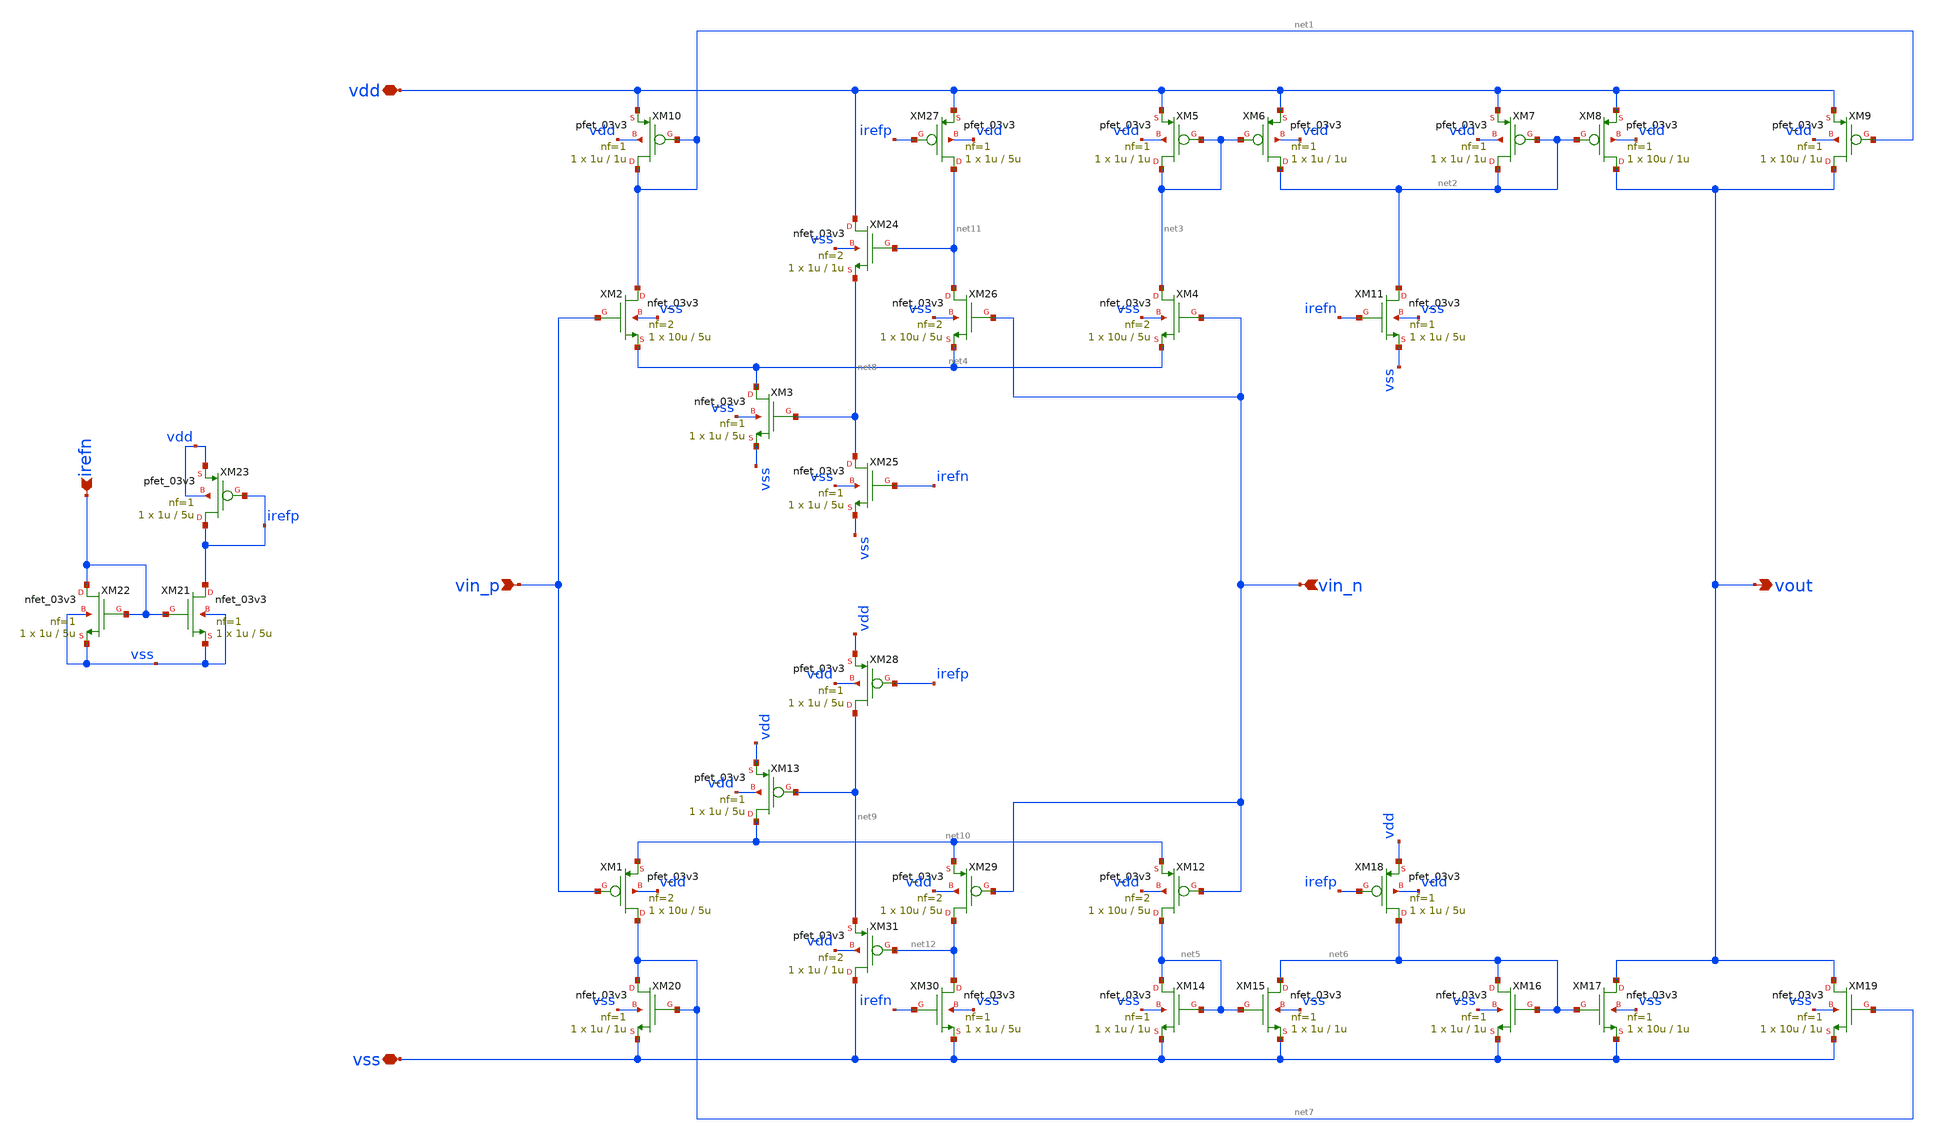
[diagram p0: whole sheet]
** sch_path: Tobias/2026 07 14 Intermediate Results/analogbuffer/analogbuffer-openloop.sch
**.subckt analogbuffer-openloop vdd vss vin_p vout irefn vin_n
*.iopin vdd
*.iopin vss
*.ipin vin_p
*.opin vout
*.ipin irefn
*.ipin vin_n
XM1 net7 vin_p net10 vdd pfet_03v3 L=5u W=10u nf=2 ad='int((nf+1)/2) * W/nf * 0.18u' as='int((nf+2)/2) * W/nf * 0.18u'
+ pd='2*int((nf+1)/2) * (W/nf + 0.18u)' ps='2*int((nf+2)/2) * (W/nf + 0.18u)' nrd='0.18u / W' nrs='0.18u / W'
+ sa=0 sb=0 sd=0 m=1
XM2 net1 vin_p net4 vss nfet_03v3 L=5u W=10u nf=2 ad='int((nf+1)/2) * W/nf * 0.18u' as='int((nf+2)/2) * W/nf * 0.18u'
+ pd='2*int((nf+1)/2) * (W/nf + 0.18u)' ps='2*int((nf+2)/2) * (W/nf + 0.18u)' nrd='0.18u / W' nrs='0.18u / W'
+ sa=0 sb=0 sd=0 m=1
XM3 net4 net8 vss vss nfet_03v3 L=5u W=1u nf=1 ad='int((nf+1)/2) * W/nf * 0.18u' as='int((nf+2)/2) * W/nf * 0.18u'
+ pd='2*int((nf+1)/2) * (W/nf + 0.18u)' ps='2*int((nf+2)/2) * (W/nf + 0.18u)' nrd='0.18u / W' nrs='0.18u / W'
+ sa=0 sb=0 sd=0 m=1
XM4 net3 vin_n net4 vss nfet_03v3 L=5u W=10u nf=2 ad='int((nf+1)/2) * W/nf * 0.18u' as='int((nf+2)/2) * W/nf * 0.18u'
+ pd='2*int((nf+1)/2) * (W/nf + 0.18u)' ps='2*int((nf+2)/2) * (W/nf + 0.18u)' nrd='0.18u / W' nrs='0.18u / W'
+ sa=0 sb=0 sd=0 m=1
XM5 net3 net3 vdd vdd pfet_03v3 L=1u W=1u nf=1 ad='int((nf+1)/2) * W/nf * 0.18u' as='int((nf+2)/2) * W/nf * 0.18u'
+ pd='2*int((nf+1)/2) * (W/nf + 0.18u)' ps='2*int((nf+2)/2) * (W/nf + 0.18u)' nrd='0.18u / W' nrs='0.18u / W'
+ sa=0 sb=0 sd=0 m=1
XM6 net2 net3 vdd vdd pfet_03v3 L=1u W=1u nf=1 ad='int((nf+1)/2) * W/nf * 0.18u' as='int((nf+2)/2) * W/nf * 0.18u'
+ pd='2*int((nf+1)/2) * (W/nf + 0.18u)' ps='2*int((nf+2)/2) * (W/nf + 0.18u)' nrd='0.18u / W' nrs='0.18u / W'
+ sa=0 sb=0 sd=0 m=1
XM7 net2 net2 vdd vdd pfet_03v3 L=1u W=1u nf=1 ad='int((nf+1)/2) * W/nf * 0.18u' as='int((nf+2)/2) * W/nf * 0.18u'
+ pd='2*int((nf+1)/2) * (W/nf + 0.18u)' ps='2*int((nf+2)/2) * (W/nf + 0.18u)' nrd='0.18u / W' nrs='0.18u / W'
+ sa=0 sb=0 sd=0 m=1
XM8 vout net2 vdd vdd pfet_03v3 L=1u W=10u nf=1 ad='int((nf+1)/2) * W/nf * 0.18u' as='int((nf+2)/2) * W/nf * 0.18u'
+ pd='2*int((nf+1)/2) * (W/nf + 0.18u)' ps='2*int((nf+2)/2) * (W/nf + 0.18u)' nrd='0.18u / W' nrs='0.18u / W'
+ sa=0 sb=0 sd=0 m=1
XM9 vout net1 vdd vdd pfet_03v3 L=1u W=10u nf=1 ad='int((nf+1)/2) * W/nf * 0.18u' as='int((nf+2)/2) * W/nf * 0.18u'
+ pd='2*int((nf+1)/2) * (W/nf + 0.18u)' ps='2*int((nf+2)/2) * (W/nf + 0.18u)' nrd='0.18u / W' nrs='0.18u / W'
+ sa=0 sb=0 sd=0 m=1
XM10 net1 net1 vdd vdd pfet_03v3 L=1u W=1u nf=1 ad='int((nf+1)/2) * W/nf * 0.18u' as='int((nf+2)/2) * W/nf * 0.18u'
+ pd='2*int((nf+1)/2) * (W/nf + 0.18u)' ps='2*int((nf+2)/2) * (W/nf + 0.18u)' nrd='0.18u / W' nrs='0.18u / W'
+ sa=0 sb=0 sd=0 m=1
XM11 net2 irefn vss vss nfet_03v3 L=5u W=1u nf=1 ad='int((nf+1)/2) * W/nf * 0.18u' as='int((nf+2)/2) * W/nf * 0.18u'
+ pd='2*int((nf+1)/2) * (W/nf + 0.18u)' ps='2*int((nf+2)/2) * (W/nf + 0.18u)' nrd='0.18u / W' nrs='0.18u / W'
+ sa=0 sb=0 sd=0 m=1
XM12 net5 vin_n net10 vdd pfet_03v3 L=5u W=10u nf=2 ad='int((nf+1)/2) * W/nf * 0.18u' as='int((nf+2)/2) * W/nf * 0.18u'
+ pd='2*int((nf+1)/2) * (W/nf + 0.18u)' ps='2*int((nf+2)/2) * (W/nf + 0.18u)' nrd='0.18u / W' nrs='0.18u / W'
+ sa=0 sb=0 sd=0 m=1
XM13 net10 net9 vdd vdd pfet_03v3 L=5u W=1u nf=1 ad='int((nf+1)/2) * W/nf * 0.18u' as='int((nf+2)/2) * W/nf * 0.18u'
+ pd='2*int((nf+1)/2) * (W/nf + 0.18u)' ps='2*int((nf+2)/2) * (W/nf + 0.18u)' nrd='0.18u / W' nrs='0.18u / W'
+ sa=0 sb=0 sd=0 m=1
XM14 net5 net5 vss vss nfet_03v3 L=1u W=1u nf=1 ad='int((nf+1)/2) * W/nf * 0.18u' as='int((nf+2)/2) * W/nf * 0.18u'
+ pd='2*int((nf+1)/2) * (W/nf + 0.18u)' ps='2*int((nf+2)/2) * (W/nf + 0.18u)' nrd='0.18u / W' nrs='0.18u / W'
+ sa=0 sb=0 sd=0 m=1
XM15 net6 net5 vss vss nfet_03v3 L=1u W=1u nf=1 ad='int((nf+1)/2) * W/nf * 0.18u' as='int((nf+2)/2) * W/nf * 0.18u'
+ pd='2*int((nf+1)/2) * (W/nf + 0.18u)' ps='2*int((nf+2)/2) * (W/nf + 0.18u)' nrd='0.18u / W' nrs='0.18u / W'
+ sa=0 sb=0 sd=0 m=1
XM16 net6 net6 vss vss nfet_03v3 L=1u W=1u nf=1 ad='int((nf+1)/2) * W/nf * 0.18u' as='int((nf+2)/2) * W/nf * 0.18u'
+ pd='2*int((nf+1)/2) * (W/nf + 0.18u)' ps='2*int((nf+2)/2) * (W/nf + 0.18u)' nrd='0.18u / W' nrs='0.18u / W'
+ sa=0 sb=0 sd=0 m=1
XM17 vout net6 vss vss nfet_03v3 L=1u W=10u nf=1 ad='int((nf+1)/2) * W/nf * 0.18u' as='int((nf+2)/2) * W/nf * 0.18u'
+ pd='2*int((nf+1)/2) * (W/nf + 0.18u)' ps='2*int((nf+2)/2) * (W/nf + 0.18u)' nrd='0.18u / W' nrs='0.18u / W'
+ sa=0 sb=0 sd=0 m=1
XM18 net6 irefp vdd vdd pfet_03v3 L=5u W=1u nf=1 ad='int((nf+1)/2) * W/nf * 0.18u' as='int((nf+2)/2) * W/nf * 0.18u'
+ pd='2*int((nf+1)/2) * (W/nf + 0.18u)' ps='2*int((nf+2)/2) * (W/nf + 0.18u)' nrd='0.18u / W' nrs='0.18u / W'
+ sa=0 sb=0 sd=0 m=1
XM19 vout net7 vss vss nfet_03v3 L=1u W=10u nf=1 ad='int((nf+1)/2) * W/nf * 0.18u' as='int((nf+2)/2) * W/nf * 0.18u'
+ pd='2*int((nf+1)/2) * (W/nf + 0.18u)' ps='2*int((nf+2)/2) * (W/nf + 0.18u)' nrd='0.18u / W' nrs='0.18u / W'
+ sa=0 sb=0 sd=0 m=1
XM20 net7 net7 vss vss nfet_03v3 L=1u W=1u nf=1 ad='int((nf+1)/2) * W/nf * 0.18u' as='int((nf+2)/2) * W/nf * 0.18u'
+ pd='2*int((nf+1)/2) * (W/nf + 0.18u)' ps='2*int((nf+2)/2) * (W/nf + 0.18u)' nrd='0.18u / W' nrs='0.18u / W'
+ sa=0 sb=0 sd=0 m=1
XM21 irefp irefn vss vss nfet_03v3 L=5u W=1u nf=1 ad='int((nf+1)/2) * W/nf * 0.18u' as='int((nf+2)/2) * W/nf * 0.18u'
+ pd='2*int((nf+1)/2) * (W/nf + 0.18u)' ps='2*int((nf+2)/2) * (W/nf + 0.18u)' nrd='0.18u / W' nrs='0.18u / W'
+ sa=0 sb=0 sd=0 m=1
XM22 irefn irefn vss vss nfet_03v3 L=5u W=1u nf=1 ad='int((nf+1)/2) * W/nf * 0.18u' as='int((nf+2)/2) * W/nf * 0.18u'
+ pd='2*int((nf+1)/2) * (W/nf + 0.18u)' ps='2*int((nf+2)/2) * (W/nf + 0.18u)' nrd='0.18u / W' nrs='0.18u / W'
+ sa=0 sb=0 sd=0 m=1
XM23 irefp irefp vdd vdd pfet_03v3 L=5u W=1u nf=1 ad='int((nf+1)/2) * W/nf * 0.18u' as='int((nf+2)/2) * W/nf * 0.18u'
+ pd='2*int((nf+1)/2) * (W/nf + 0.18u)' ps='2*int((nf+2)/2) * (W/nf + 0.18u)' nrd='0.18u / W' nrs='0.18u / W'
+ sa=0 sb=0 sd=0 m=1
XM24 vdd net11 net8 vss nfet_03v3 L=1u W=1u nf=2 ad='int((nf+1)/2) * W/nf * 0.18u' as='int((nf+2)/2) * W/nf * 0.18u'
+ pd='2*int((nf+1)/2) * (W/nf + 0.18u)' ps='2*int((nf+2)/2) * (W/nf + 0.18u)' nrd='0.18u / W' nrs='0.18u / W'
+ sa=0 sb=0 sd=0 m=1
XM25 net8 irefn vss vss nfet_03v3 L=5u W=1u nf=1 ad='int((nf+1)/2) * W/nf * 0.18u' as='int((nf+2)/2) * W/nf * 0.18u'
+ pd='2*int((nf+1)/2) * (W/nf + 0.18u)' ps='2*int((nf+2)/2) * (W/nf + 0.18u)' nrd='0.18u / W' nrs='0.18u / W'
+ sa=0 sb=0 sd=0 m=1
XM26 net11 vin_n net4 vss nfet_03v3 L=5u W=10u nf=2 ad='int((nf+1)/2) * W/nf * 0.18u' as='int((nf+2)/2) * W/nf * 0.18u'
+ pd='2*int((nf+1)/2) * (W/nf + 0.18u)' ps='2*int((nf+2)/2) * (W/nf + 0.18u)' nrd='0.18u / W' nrs='0.18u / W'
+ sa=0 sb=0 sd=0 m=1
XM27 net11 irefp vdd vdd pfet_03v3 L=5u W=1u nf=1 ad='int((nf+1)/2) * W/nf * 0.18u' as='int((nf+2)/2) * W/nf * 0.18u'
+ pd='2*int((nf+1)/2) * (W/nf + 0.18u)' ps='2*int((nf+2)/2) * (W/nf + 0.18u)' nrd='0.18u / W' nrs='0.18u / W'
+ sa=0 sb=0 sd=0 m=1
XM28 net9 irefp vdd vdd pfet_03v3 L=5u W=1u nf=1 ad='int((nf+1)/2) * W/nf * 0.18u' as='int((nf+2)/2) * W/nf * 0.18u'
+ pd='2*int((nf+1)/2) * (W/nf + 0.18u)' ps='2*int((nf+2)/2) * (W/nf + 0.18u)' nrd='0.18u / W' nrs='0.18u / W'
+ sa=0 sb=0 sd=0 m=1
XM29 net12 vin_n net10 vdd pfet_03v3 L=5u W=10u nf=2 ad='int((nf+1)/2) * W/nf * 0.18u' as='int((nf+2)/2) * W/nf * 0.18u'
+ pd='2*int((nf+1)/2) * (W/nf + 0.18u)' ps='2*int((nf+2)/2) * (W/nf + 0.18u)' nrd='0.18u / W' nrs='0.18u / W'
+ sa=0 sb=0 sd=0 m=1
XM30 net12 irefn vss vss nfet_03v3 L=5u W=1u nf=1 ad='int((nf+1)/2) * W/nf * 0.18u' as='int((nf+2)/2) * W/nf * 0.18u'
+ pd='2*int((nf+1)/2) * (W/nf + 0.18u)' ps='2*int((nf+2)/2) * (W/nf + 0.18u)' nrd='0.18u / W' nrs='0.18u / W'
+ sa=0 sb=0 sd=0 m=1
XM31 vss net12 net9 vdd pfet_03v3 L=1u W=1u nf=2 ad='int((nf+1)/2) * W/nf * 0.18u' as='int((nf+2)/2) * W/nf * 0.18u'
+ pd='2*int((nf+1)/2) * (W/nf + 0.18u)' ps='2*int((nf+2)/2) * (W/nf + 0.18u)' nrd='0.18u / W' nrs='0.18u / W'
+ sa=0 sb=0 sd=0 m=1
**.ends
.end
